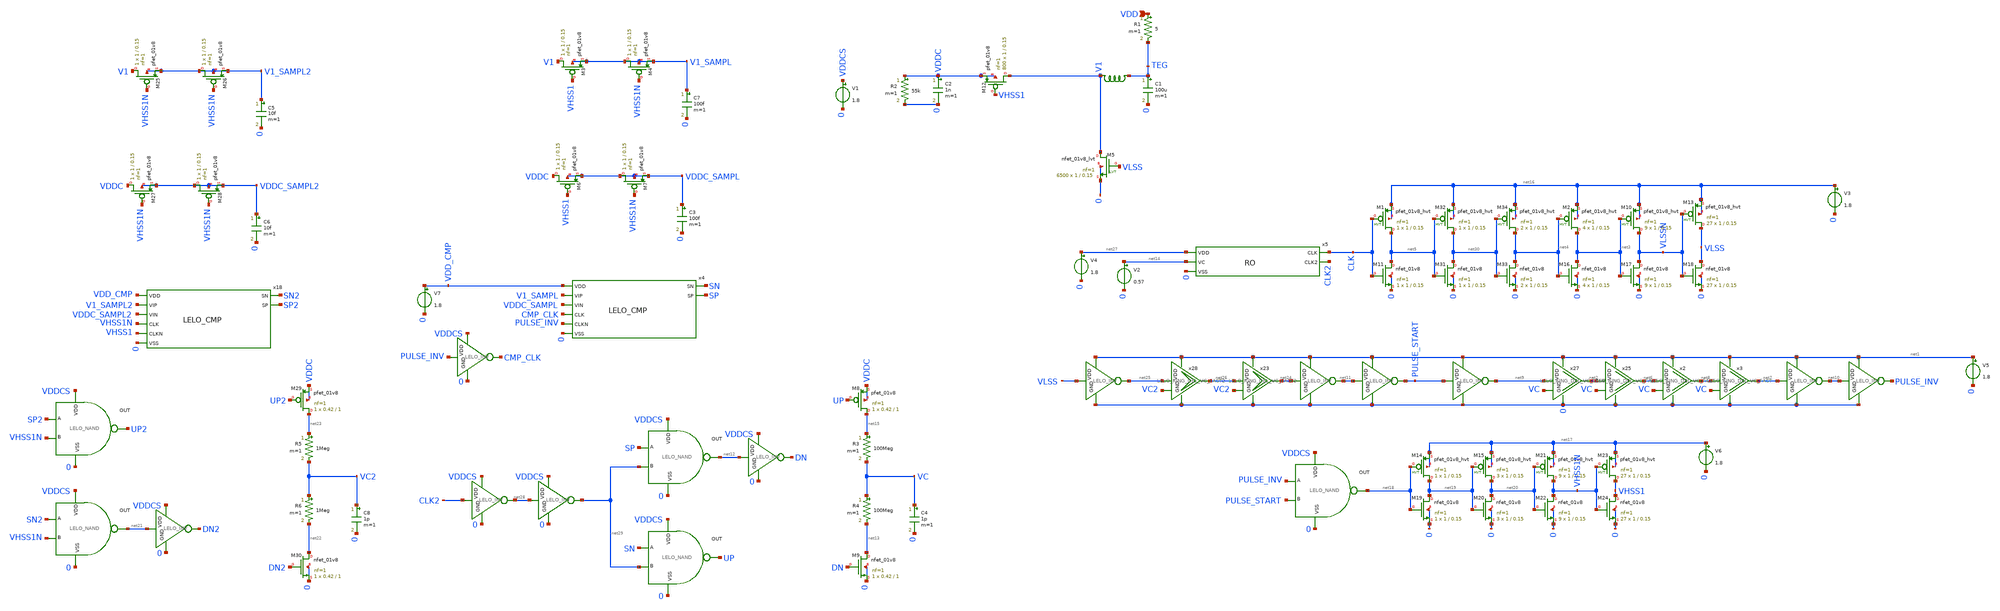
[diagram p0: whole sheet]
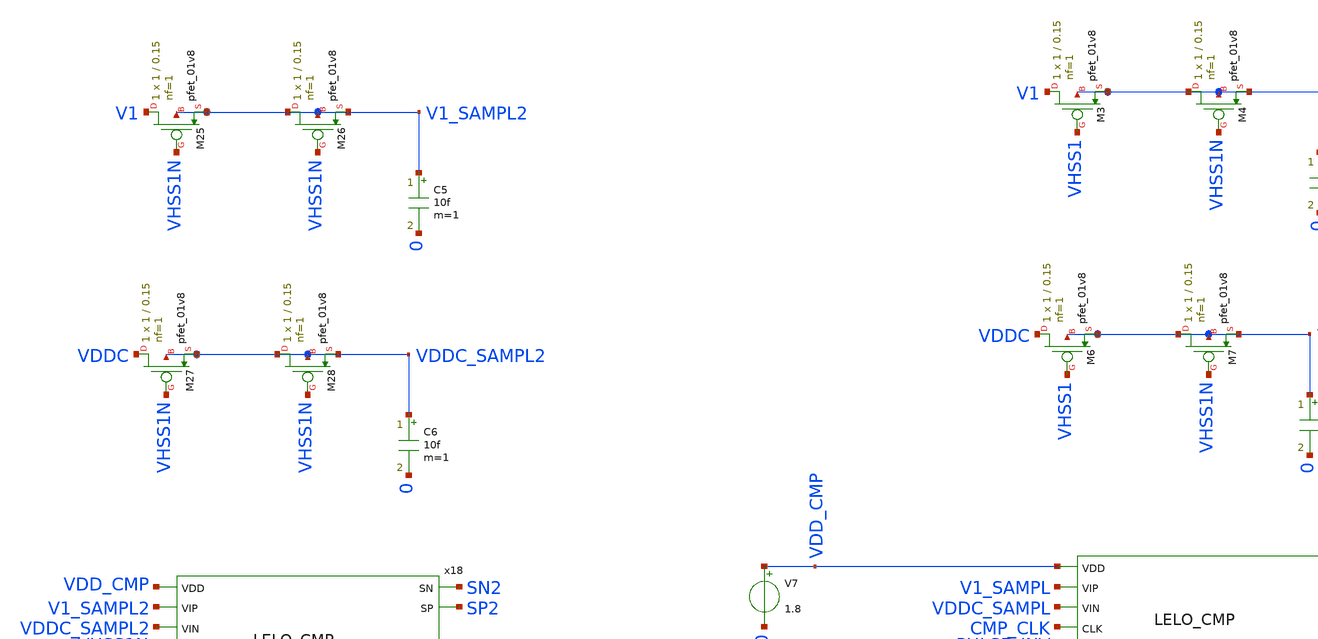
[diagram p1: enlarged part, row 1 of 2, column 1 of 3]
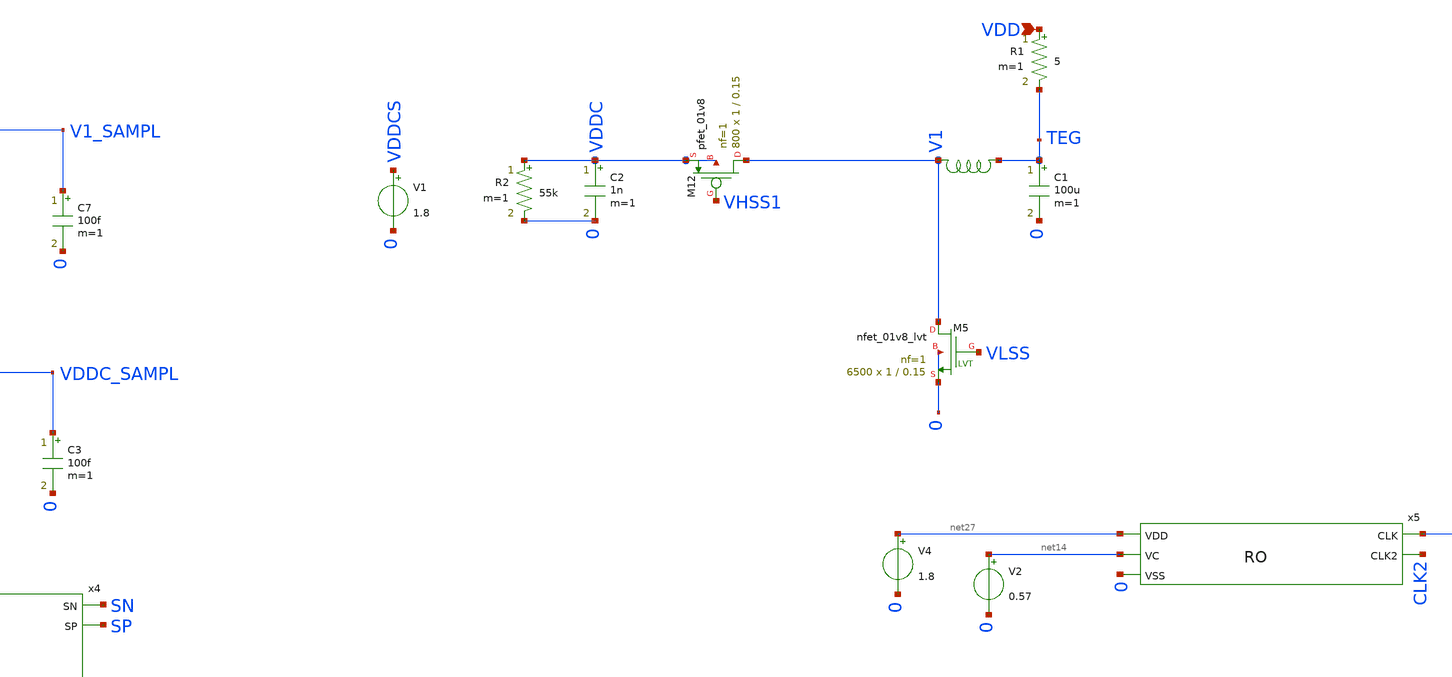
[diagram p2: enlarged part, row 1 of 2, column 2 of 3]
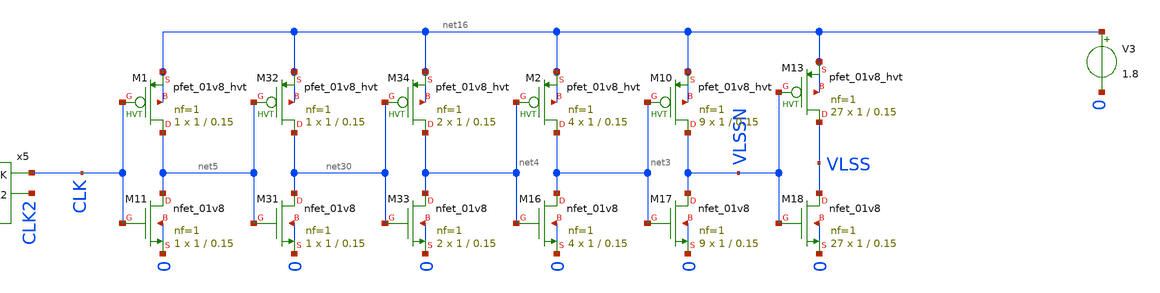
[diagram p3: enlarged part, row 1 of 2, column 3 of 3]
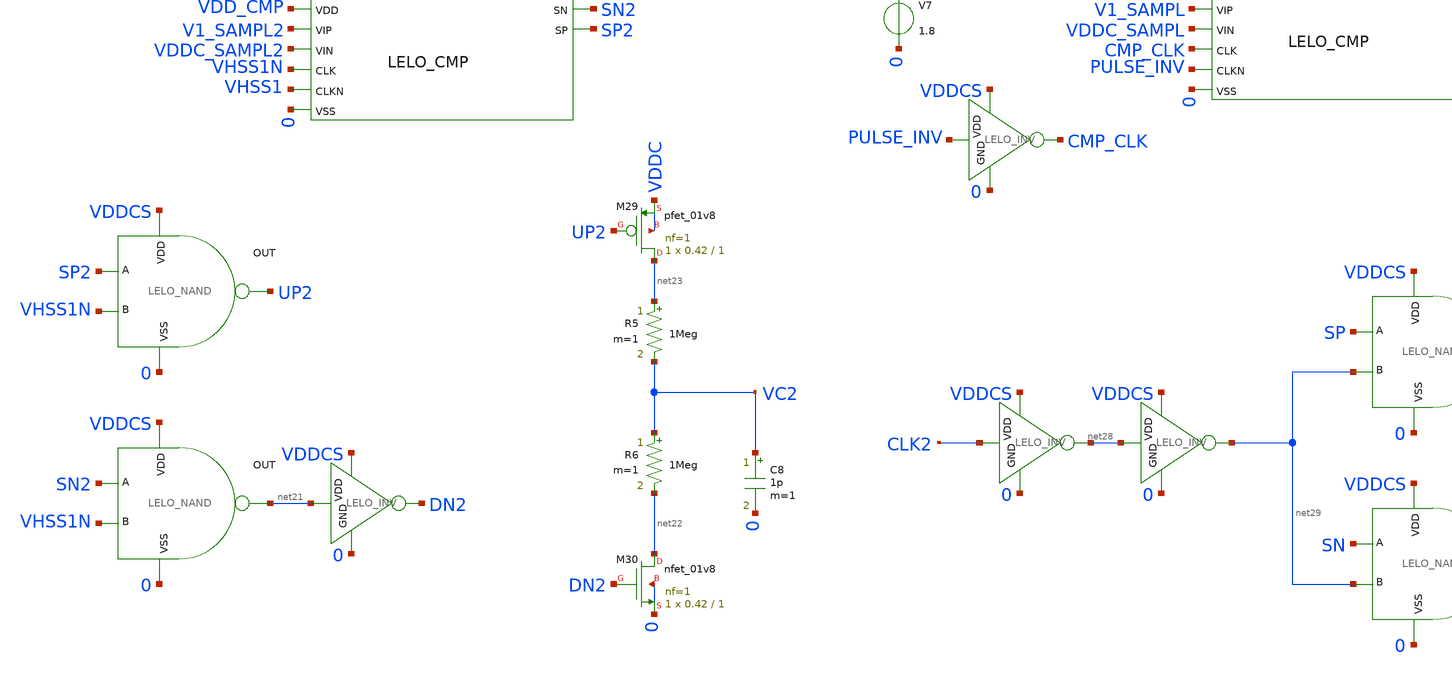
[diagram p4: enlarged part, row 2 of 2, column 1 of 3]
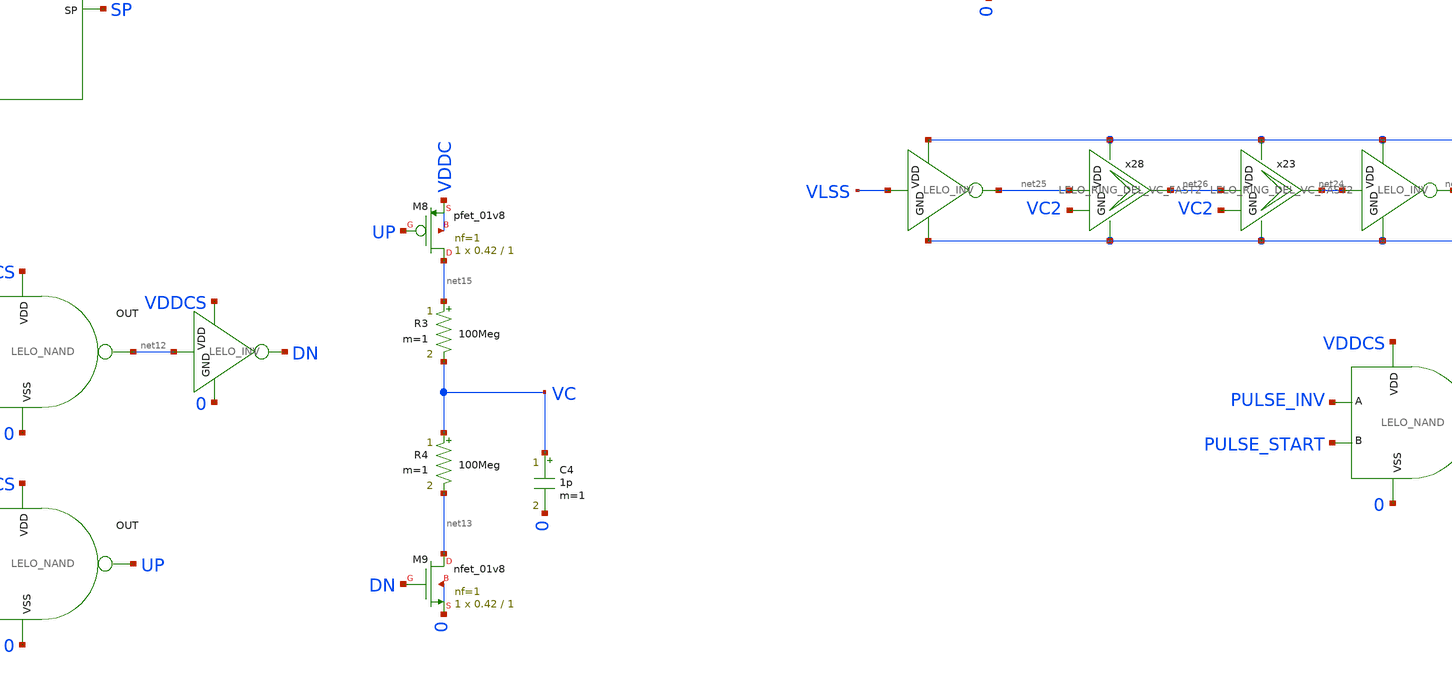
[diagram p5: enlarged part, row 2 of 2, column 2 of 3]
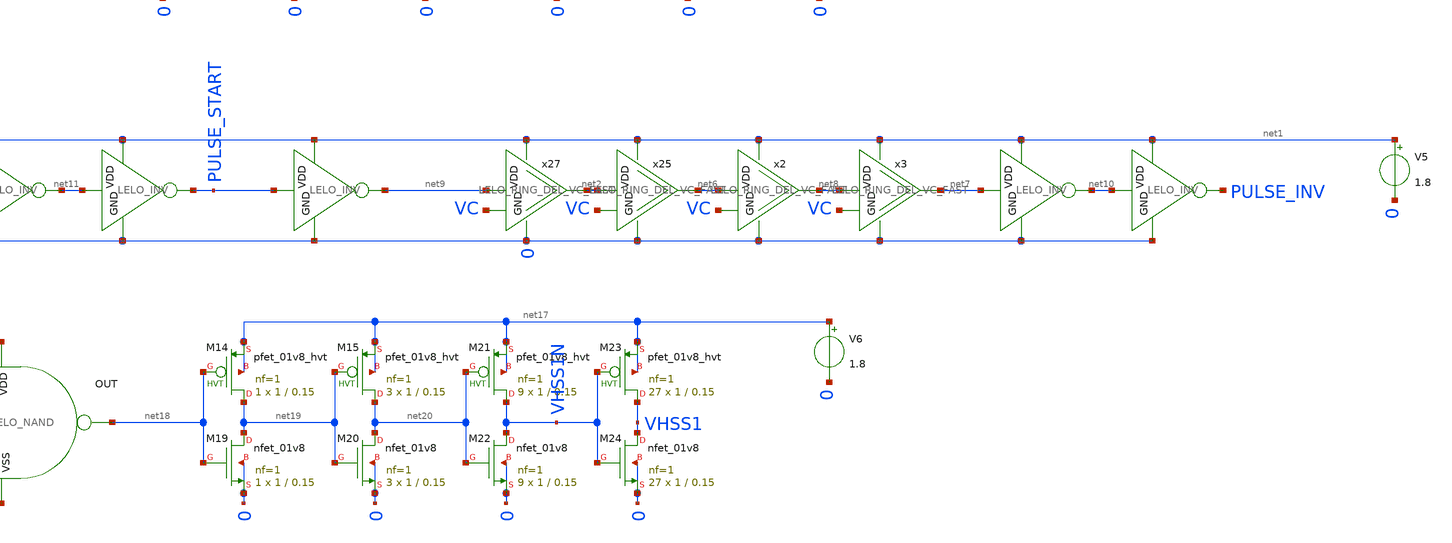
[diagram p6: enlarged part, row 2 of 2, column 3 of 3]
** sch_path: design/LELO_SVOD_SKY130A/LELO_BOOST_STEADY_STATE.sch
**.subckt LELO_BOOST_STEADY_STATE VDD
*.ipin VDD
R1 VDD TEG 5 m=1
C7 V1_SAMPL 0 100f m=1
x8 VDDCS net18 PULSE_INV PULSE_START 0 LELO_NAND
x25 net1 net2 net6 0 VC LELO_RING_DEL_VC_FAST
x6 net1 net7 net10 0 LELO_INV
x27 net1 net9 net2 0 VC LELO_RING_DEL_VC_FAST
x5 CLK CLK2 net27 net14 0 RO
XM12 V1 VHSS1 VDDC VDDC sky130_fd_pr__pfet_01v8 L=0.15 W=1 nf=1 ad='int((1 + 1)/2) * 1 / 1 * 0.29' as='int((1 + 2)/2) * 1 / 1 * 0.29'
+ pd='2*int((1 + 1)/2) * (1 / 1 + 0.29)' ps='2*int((1 + 2)/2) * (1 / 1 + 0.29)' nrd='0.29 / 1 ' nrs='0.29 / 1 '
+ sa=0 sb=0 sd=0 mult=800 m=800
x2 net1 net6 net8 0 VC LELO_RING_DEL_VC_FAST
x3 net1 net8 net7 0 VC LELO_RING_DEL_VC_FAST
x1 net1 net24 net11 0 LELO_INV
x16 net1 net10 PULSE_INV 0 LELO_INV
C1 TEG 0 100u m=1
x9 net1 VLSS net25 0 LELO_INV
XM5 V1 VLSS 0 0 sky130_fd_pr__nfet_01v8_lvt L=0.15 W=1 nf=1 ad='int((1 + 1)/2) * 1 / 1 * 0.29' as='int((1 + 2)/2) * 1 / 1 * 0.29'
+ pd='2*int((1 + 1)/2) * (1 / 1 + 0.29)' ps='2*int((1 + 2)/2) * (1 / 1 + 0.29)' nrd='0.29 / 1 ' nrs='0.29 / 1 '
+ sa=0 sb=0 sd=0 mult=6500 m=6500
C2 VDDC 0 1n m=1
V1 VDDCS 0 1.8
R2 VDDC 0 55k m=1
x4 SN SP VDD_CMP V1_SAMPL VDDC_SAMPL CMP_CLK PULSE_INV 0 LELO_CMP
XM3 V1 VHSS1 V1_SAMPL V1_SAMPL sky130_fd_pr__pfet_01v8 L=0.15 W=1 nf=1 ad='int((1 + 1)/2) * 1 / 1 * 0.29'
+ as='int((1 + 2)/2) * 1 / 1 * 0.29' pd='2*int((1 + 1)/2) * (1 / 1 + 0.29)' ps='2*int((1 + 2)/2) * (1 / 1 + 0.29)'
+ nrd='0.29 / 1 ' nrs='0.29 / 1 ' sa=0 sb=0 sd=0 mult=1 m=1
XM4 V1_SAMPL VHSS1N V1_SAMPL V1_SAMPL sky130_fd_pr__pfet_01v8 L=0.15 W=1 nf=1 ad='int((1 + 1)/2) * 1 / 1 * 0.29'
+ as='int((1 + 2)/2) * 1 / 1 * 0.29' pd='2*int((1 + 1)/2) * (1 / 1 + 0.29)' ps='2*int((1 + 2)/2) * (1 / 1 + 0.29)'
+ nrd='0.29 / 1 ' nrs='0.29 / 1 ' sa=0 sb=0 sd=0 mult=1 m=1
C3 VDDC_SAMPL 0 100f m=1
XM6 VDDC VHSS1 VDDC_SAMPL VDDC_SAMPL sky130_fd_pr__pfet_01v8 L=0.15 W=1 nf=1 ad='int((1 + 1)/2) * 1 / 1 * 0.29'
+ as='int((1 + 2)/2) * 1 / 1 * 0.29' pd='2*int((1 + 1)/2) * (1 / 1 + 0.29)' ps='2*int((1 + 2)/2) * (1 / 1 + 0.29)'
+ nrd='0.29 / 1 ' nrs='0.29 / 1 ' sa=0 sb=0 sd=0 mult=1 m=1
XM7 VDDC_SAMPL VHSS1N VDDC_SAMPL VDDC_SAMPL sky130_fd_pr__pfet_01v8 L=0.15 W=1 nf=1 ad='int((1 + 1)/2) * 1 / 1 * 0.29'
+ as='int((1 + 2)/2) * 1 / 1 * 0.29' pd='2*int((1 + 1)/2) * (1 / 1 + 0.29)' ps='2*int((1 + 2)/2) * (1 / 1 + 0.29)'
+ nrd='0.29 / 1 ' nrs='0.29 / 1 ' sa=0 sb=0 sd=0 mult=1 m=1
C4 VC 0 1p m=1
XM8 net15 UP VDDC VDDC sky130_fd_pr__pfet_01v8 L=1 W=0.42 nf=1 ad='int((1 + 1)/2) * 0.42 / 1 * 0.29'
+ as='int((1 + 2)/2) * 0.42 / 1 * 0.29' pd='2*int((1 + 1)/2) * (0.42 / 1 + 0.29)' ps='2*int((1 + 2)/2) * (0.42 / 1 + 0.29)'
+ nrd='0.29 / 0.42 ' nrs='0.29 / 0.42 ' sa=0 sb=0 sd=0 mult=1 m=1
XM9 net13 DN 0 0 sky130_fd_pr__nfet_01v8 L=1 W=0.42 nf=1 ad='int((1 + 1)/2) * 0.42 / 1 * 0.29' as='int((1 + 2)/2) * 0.42 / 1 * 0.29'
+ pd='2*int((1 + 1)/2) * (0.42 / 1 + 0.29)' ps='2*int((1 + 2)/2) * (0.42 / 1 + 0.29)' nrd='0.29 / 0.42 '
+ nrs='0.29 / 0.42 ' sa=0 sb=0 sd=0 mult=1 m=1
x10 VDDCS net12 SP net29 0 LELO_NAND
x11 VDDCS net12 DN 0 LELO_INV
x12 VDDCS UP SN net29 0 LELO_NAND
V2 net14 0 0.57
x14 VDDCS PULSE_INV CMP_CLK 0 LELO_INV
R3 net15 VC 100Meg m=1
R4 VC net13 100Meg m=1
XM11 net5 CLK 0 0 sky130_fd_pr__nfet_01v8 L=0.15 W=1 nf=1 ad='int((1 + 1)/2) * 1 / 1 * 0.29' as='int((1 + 2)/2) * 1 / 1 * 0.29'
+ pd='2*int((1 + 1)/2) * (1 / 1 + 0.29)' ps='2*int((1 + 2)/2) * (1 / 1 + 0.29)' nrd='0.29 / 1 ' nrs='0.29 / 1 '
+ sa=0 sb=0 sd=0 mult=1 m=1
XM16 net3 net4 0 0 sky130_fd_pr__nfet_01v8 L=0.15 W=1 nf=1 ad='int((1 + 1)/2) * 1 / 1 * 0.29' as='int((1 + 2)/2) * 1 / 1 * 0.29'
+ pd='2*int((1 + 1)/2) * (1 / 1 + 0.29)' ps='2*int((1 + 2)/2) * (1 / 1 + 0.29)' nrd='0.29 / 1 ' nrs='0.29 / 1 '
+ sa=0 sb=0 sd=0 mult=4 m=4
XM17 VLSSN net3 0 0 sky130_fd_pr__nfet_01v8 L=0.15 W=1 nf=1 ad='int((1 + 1)/2) * 1 / 1 * 0.29' as='int((1 + 2)/2) * 1 / 1 * 0.29'
+ pd='2*int((1 + 1)/2) * (1 / 1 + 0.29)' ps='2*int((1 + 2)/2) * (1 / 1 + 0.29)' nrd='0.29 / 1 ' nrs='0.29 / 1 '
+ sa=0 sb=0 sd=0 mult=9 m=9
XM18 VLSS VLSSN 0 0 sky130_fd_pr__nfet_01v8 L=0.15 W=1 nf=1 ad='int((1 + 1)/2) * 1 / 1 * 0.29' as='int((1 + 2)/2) * 1 / 1 * 0.29'
+ pd='2*int((1 + 1)/2) * (1 / 1 + 0.29)' ps='2*int((1 + 2)/2) * (1 / 1 + 0.29)' nrd='0.29 / 1 ' nrs='0.29 / 1 '
+ sa=0 sb=0 sd=0 mult=27 m=27
XM19 net19 net18 0 0 sky130_fd_pr__nfet_01v8 L=0.15 W=1 nf=1 ad='int((1 + 1)/2) * 1 / 1 * 0.29' as='int((1 + 2)/2) * 1 / 1 * 0.29'
+ pd='2*int((1 + 1)/2) * (1 / 1 + 0.29)' ps='2*int((1 + 2)/2) * (1 / 1 + 0.29)' nrd='0.29 / 1 ' nrs='0.29 / 1 '
+ sa=0 sb=0 sd=0 mult=1 m=1
XM20 net20 net19 0 0 sky130_fd_pr__nfet_01v8 L=0.15 W=1 nf=1 ad='int((1 + 1)/2) * 1 / 1 * 0.29' as='int((1 + 2)/2) * 1 / 1 * 0.29'
+ pd='2*int((1 + 1)/2) * (1 / 1 + 0.29)' ps='2*int((1 + 2)/2) * (1 / 1 + 0.29)' nrd='0.29 / 1 ' nrs='0.29 / 1 '
+ sa=0 sb=0 sd=0 mult=3 m=3
XM22 VHSS1N net20 0 0 sky130_fd_pr__nfet_01v8 L=0.15 W=1 nf=1 ad='int((1 + 1)/2) * 1 / 1 * 0.29' as='int((1 + 2)/2) * 1 / 1 * 0.29'
+ pd='2*int((1 + 1)/2) * (1 / 1 + 0.29)' ps='2*int((1 + 2)/2) * (1 / 1 + 0.29)' nrd='0.29 / 1 ' nrs='0.29 / 1 '
+ sa=0 sb=0 sd=0 mult=9 m=9
XM24 VHSS1 VHSS1N 0 0 sky130_fd_pr__nfet_01v8 L=0.15 W=1 nf=1 ad='int((1 + 1)/2) * 1 / 1 * 0.29' as='int((1 + 2)/2) * 1 / 1 * 0.29'
+ pd='2*int((1 + 1)/2) * (1 / 1 + 0.29)' ps='2*int((1 + 2)/2) * (1 / 1 + 0.29)' nrd='0.29 / 1 ' nrs='0.29 / 1 '
+ sa=0 sb=0 sd=0 mult=27 m=27
XM1 net5 CLK net16 net16 sky130_fd_pr__pfet_01v8_hvt L=0.15 W=1 nf=1 ad='int((1 + 1)/2) * 1 / 1 * 0.29'
+ as='int((1 + 2)/2) * 1 / 1 * 0.29' pd='2*int((1 + 1)/2) * (1 / 1 + 0.29)' ps='2*int((1 + 2)/2) * (1 / 1 + 0.29)'
+ nrd='0.29 / 1 ' nrs='0.29 / 1 ' sa=0 sb=0 sd=0 mult=1 m=1
XM2 net3 net4 net16 net16 sky130_fd_pr__pfet_01v8_hvt L=0.15 W=1 nf=1 ad='int((1 + 1)/2) * 1 / 1 * 0.29'
+ as='int((1 + 2)/2) * 1 / 1 * 0.29' pd='2*int((1 + 1)/2) * (1 / 1 + 0.29)' ps='2*int((1 + 2)/2) * (1 / 1 + 0.29)'
+ nrd='0.29 / 1 ' nrs='0.29 / 1 ' sa=0 sb=0 sd=0 mult=4 m=4
XM10 VLSSN net3 net16 net16 sky130_fd_pr__pfet_01v8_hvt L=0.15 W=1 nf=1 ad='int((1 + 1)/2) * 1 / 1 * 0.29'
+ as='int((1 + 2)/2) * 1 / 1 * 0.29' pd='2*int((1 + 1)/2) * (1 / 1 + 0.29)' ps='2*int((1 + 2)/2) * (1 / 1 + 0.29)'
+ nrd='0.29 / 1 ' nrs='0.29 / 1 ' sa=0 sb=0 sd=0 mult=9 m=9
XM13 VLSS VLSSN net16 net16 sky130_fd_pr__pfet_01v8_hvt L=0.15 W=1 nf=1 ad='int((1 + 1)/2) * 1 / 1 * 0.29'
+ as='int((1 + 2)/2) * 1 / 1 * 0.29' pd='2*int((1 + 1)/2) * (1 / 1 + 0.29)' ps='2*int((1 + 2)/2) * (1 / 1 + 0.29)'
+ nrd='0.29 / 1 ' nrs='0.29 / 1 ' sa=0 sb=0 sd=0 mult=27 m=27
XM14 net19 net18 net17 net17 sky130_fd_pr__pfet_01v8_hvt L=0.15 W=1 nf=1 ad='int((1 + 1)/2) * 1 / 1 * 0.29'
+ as='int((1 + 2)/2) * 1 / 1 * 0.29' pd='2*int((1 + 1)/2) * (1 / 1 + 0.29)' ps='2*int((1 + 2)/2) * (1 / 1 + 0.29)'
+ nrd='0.29 / 1 ' nrs='0.29 / 1 ' sa=0 sb=0 sd=0 mult=1 m=1
XM15 net20 net19 net17 net17 sky130_fd_pr__pfet_01v8_hvt L=0.15 W=1 nf=1 ad='int((1 + 1)/2) * 1 / 1 * 0.29'
+ as='int((1 + 2)/2) * 1 / 1 * 0.29' pd='2*int((1 + 1)/2) * (1 / 1 + 0.29)' ps='2*int((1 + 2)/2) * (1 / 1 + 0.29)'
+ nrd='0.29 / 1 ' nrs='0.29 / 1 ' sa=0 sb=0 sd=0 mult=3 m=3
XM21 VHSS1N net20 net17 net17 sky130_fd_pr__pfet_01v8_hvt L=0.15 W=1 nf=1 ad='int((1 + 1)/2) * 1 / 1 * 0.29'
+ as='int((1 + 2)/2) * 1 / 1 * 0.29' pd='2*int((1 + 1)/2) * (1 / 1 + 0.29)' ps='2*int((1 + 2)/2) * (1 / 1 + 0.29)'
+ nrd='0.29 / 1 ' nrs='0.29 / 1 ' sa=0 sb=0 sd=0 mult=9 m=9
XM23 VHSS1 VHSS1N net17 net17 sky130_fd_pr__pfet_01v8_hvt L=0.15 W=1 nf=1 ad='int((1 + 1)/2) * 1 / 1 * 0.29'
+ as='int((1 + 2)/2) * 1 / 1 * 0.29' pd='2*int((1 + 1)/2) * (1 / 1 + 0.29)' ps='2*int((1 + 2)/2) * (1 / 1 + 0.29)'
+ nrd='0.29 / 1 ' nrs='0.29 / 1 ' sa=0 sb=0 sd=0 mult=27 m=27
C5 V1_SAMPL2 0 10f m=1
x18 SN2 SP2 VDD_CMP V1_SAMPL2 VDDC_SAMPL2 VHSS1N VHSS1 0 LELO_CMP
XM25 V1 VHSS1N V1_SAMPL2 V1_SAMPL2 sky130_fd_pr__pfet_01v8 L=0.15 W=1 nf=1 ad='int((1 + 1)/2) * 1 / 1 * 0.29'
+ as='int((1 + 2)/2) * 1 / 1 * 0.29' pd='2*int((1 + 1)/2) * (1 / 1 + 0.29)' ps='2*int((1 + 2)/2) * (1 / 1 + 0.29)'
+ nrd='0.29 / 1 ' nrs='0.29 / 1 ' sa=0 sb=0 sd=0 mult=1 m=1
XM26 V1_SAMPL2 VHSS1N V1_SAMPL2 V1_SAMPL2 sky130_fd_pr__pfet_01v8 L=0.15 W=1 nf=1 ad='int((1 + 1)/2) * 1 / 1 * 0.29'
+ as='int((1 + 2)/2) * 1 / 1 * 0.29' pd='2*int((1 + 1)/2) * (1 / 1 + 0.29)' ps='2*int((1 + 2)/2) * (1 / 1 + 0.29)'
+ nrd='0.29 / 1 ' nrs='0.29 / 1 ' sa=0 sb=0 sd=0 mult=1 m=1
C6 VDDC_SAMPL2 0 10f m=1
XM27 VDDC VHSS1N VDDC_SAMPL2 VDDC_SAMPL2 sky130_fd_pr__pfet_01v8 L=0.15 W=1 nf=1 ad='int((1 + 1)/2) * 1 / 1 * 0.29'
+ as='int((1 + 2)/2) * 1 / 1 * 0.29' pd='2*int((1 + 1)/2) * (1 / 1 + 0.29)' ps='2*int((1 + 2)/2) * (1 / 1 + 0.29)'
+ nrd='0.29 / 1 ' nrs='0.29 / 1 ' sa=0 sb=0 sd=0 mult=1 m=1
XM28 VDDC_SAMPL2 VHSS1N VDDC_SAMPL2 VDDC_SAMPL2 sky130_fd_pr__pfet_01v8 L=0.15 W=1 nf=1 ad='int((1 + 1)/2) * 1 / 1 * 0.29'
+ as='int((1 + 2)/2) * 1 / 1 * 0.29' pd='2*int((1 + 1)/2) * (1 / 1 + 0.29)' ps='2*int((1 + 2)/2) * (1 / 1 + 0.29)'
+ nrd='0.29 / 1 ' nrs='0.29 / 1 ' sa=0 sb=0 sd=0 mult=1 m=1
x19 VDDCS UP2 SP2 VHSS1N 0 LELO_NAND
x20 VDDCS net21 DN2 0 LELO_INV
x21 VDDCS net21 SN2 VHSS1N 0 LELO_NAND
C8 VC2 0 1p m=1
XM29 net23 UP2 VDDC VDDC sky130_fd_pr__pfet_01v8 L=1 W=0.42 nf=1 ad='int((1 + 1)/2) * 0.42 / 1 * 0.29'
+ as='int((1 + 2)/2) * 0.42 / 1 * 0.29' pd='2*int((1 + 1)/2) * (0.42 / 1 + 0.29)' ps='2*int((1 + 2)/2) * (0.42 / 1 + 0.29)'
+ nrd='0.29 / 0.42 ' nrs='0.29 / 0.42 ' sa=0 sb=0 sd=0 mult=1 m=1
XM30 net22 DN2 0 0 sky130_fd_pr__nfet_01v8 L=1 W=0.42 nf=1 ad='int((1 + 1)/2) * 0.42 / 1 * 0.29' as='int((1 + 2)/2) * 0.42 / 1 * 0.29'
+ pd='2*int((1 + 1)/2) * (0.42 / 1 + 0.29)' ps='2*int((1 + 2)/2) * (0.42 / 1 + 0.29)' nrd='0.29 / 0.42 '
+ nrs='0.29 / 0.42 ' sa=0 sb=0 sd=0 mult=1 m=1
R5 net23 VC2 1Meg m=1
R6 VC2 net22 1Meg m=1
x23 net1 net26 net24 0 VC2 LELO_RING_DEL_VC_FAST2
x28 net1 net25 net26 0 VC2 LELO_RING_DEL_VC_FAST2
V4 net27 0 1.8
V3 net16 0 1.8
V5 net1 0 1.8
V6 net17 0 1.8
V7 VDD_CMP 0 1.8
x13 VDDCS net28 net29 0 LELO_INV
x15 VDDCS CLK2 net28 0 LELO_INV
x17 net1 net11 PULSE_START 0 LELO_INV
x22 net1 PULSE_START net9 0 LELO_INV
XM31 net30 net5 0 0 sky130_fd_pr__nfet_01v8 L=0.15 W=1 nf=1 ad='int((1 + 1)/2) * 1 / 1 * 0.29' as='int((1 + 2)/2) * 1 / 1 * 0.29'
+ pd='2*int((1 + 1)/2) * (1 / 1 + 0.29)' ps='2*int((1 + 2)/2) * (1 / 1 + 0.29)' nrd='0.29 / 1 ' nrs='0.29 / 1 '
+ sa=0 sb=0 sd=0 mult=1 m=1
XM32 net30 net5 net16 net16 sky130_fd_pr__pfet_01v8_hvt L=0.15 W=1 nf=1 ad='int((1 + 1)/2) * 1 / 1 * 0.29'
+ as='int((1 + 2)/2) * 1 / 1 * 0.29' pd='2*int((1 + 1)/2) * (1 / 1 + 0.29)' ps='2*int((1 + 2)/2) * (1 / 1 + 0.29)'
+ nrd='0.29 / 1 ' nrs='0.29 / 1 ' sa=0 sb=0 sd=0 mult=1 m=1
XM33 net4 net30 0 0 sky130_fd_pr__nfet_01v8 L=0.15 W=1 nf=1 ad='int((1 + 1)/2) * 1 / 1 * 0.29' as='int((1 + 2)/2) * 1 / 1 * 0.29'
+ pd='2*int((1 + 1)/2) * (1 / 1 + 0.29)' ps='2*int((1 + 2)/2) * (1 / 1 + 0.29)' nrd='0.29 / 1 ' nrs='0.29 / 1 '
+ sa=0 sb=0 sd=0 mult=2 m=2
XM34 net4 net30 net16 net16 sky130_fd_pr__pfet_01v8_hvt L=0.15 W=1 nf=1 ad='int((1 + 1)/2) * 1 / 1 * 0.29'
+ as='int((1 + 2)/2) * 1 / 1 * 0.29' pd='2*int((1 + 1)/2) * (1 / 1 + 0.29)' ps='2*int((1 + 2)/2) * (1 / 1 + 0.29)'
+ nrd='0.29 / 1 ' nrs='0.29 / 1 ' sa=0 sb=0 sd=0 mult=2 m=2
x7 TEG V1 XGL6030-822_sat
**.ends

* expanding   symbol:  LELO_SVOD_SKY130A/LELO_NAND.sym # of pins=5
** sym_path: design/LELO_SVOD_SKY130A/LELO_NAND.sym
** sch_path: design/LELO_SVOD_SKY130A/LELO_NAND.sch
.subckt LELO_NAND VDD OUT A B VSS
*.ipin VDD
*.ipin VSS
*.opin OUT
*.ipin A
*.ipin B
XM1 net1 A VSS VSS sky130_fd_pr__nfet_01v8_lvt L=0.15 W=1 nf=1 ad='int((1 + 1)/2) * 1 / 1 * 0.29' as='int((1 + 2)/2) * 1 / 1 * 0.29'
+ pd='2*int((1 + 1)/2) * (1 / 1 + 0.29)' ps='2*int((1 + 2)/2) * (1 / 1 + 0.29)' nrd='0.29 / 1 ' nrs='0.29 / 1 '
+ sa=0 sb=0 sd=0 mult=1 m=1
XM2 OUT B net1 net1 sky130_fd_pr__nfet_01v8_lvt L=0.15 W=1 nf=1 ad='int((1 + 1)/2) * 1 / 1 * 0.29' as='int((1 + 2)/2) * 1 / 1 * 0.29'
+ pd='2*int((1 + 1)/2) * (1 / 1 + 0.29)' ps='2*int((1 + 2)/2) * (1 / 1 + 0.29)' nrd='0.29 / 1 ' nrs='0.29 / 1 '
+ sa=0 sb=0 sd=0 mult=1 m=1
XM3 OUT A VDD VDD sky130_fd_pr__pfet_01v8_lvt L=0.35 W=1 nf=1 ad='int((1 + 1)/2) * 1 / 1 * 0.29' as='int((1 + 2)/2) * 1 / 1 * 0.29'
+ pd='2*int((1 + 1)/2) * (1 / 1 + 0.29)' ps='2*int((1 + 2)/2) * (1 / 1 + 0.29)' nrd='0.29 / 1 ' nrs='0.29 / 1 '
+ sa=0 sb=0 sd=0 mult=1 m=1
XM4 OUT B VDD VDD sky130_fd_pr__pfet_01v8_lvt L=0.35 W=1 nf=1 ad='int((1 + 1)/2) * 1 / 1 * 0.29' as='int((1 + 2)/2) * 1 / 1 * 0.29'
+ pd='2*int((1 + 1)/2) * (1 / 1 + 0.29)' ps='2*int((1 + 2)/2) * (1 / 1 + 0.29)' nrd='0.29 / 1 ' nrs='0.29 / 1 '
+ sa=0 sb=0 sd=0 mult=1 m=1
.ends


* expanding   symbol:  LELO_SVOD_SKY130A/LELO_RING_DEL_VC_FAST.sym # of pins=5
** sym_path: design/LELO_SVOD_SKY130A/LELO_RING_DEL_VC_FAST.sym
** sch_path: design/LELO_SVOD_SKY130A/LELO_RING_DEL_VC_FAST.sch
.subckt LELO_RING_DEL_VC_FAST VDD VIN VOUT GND VC
*.ipin VIN
*.ipin VDD
*.opin VOUT
*.ipin VC
*.ipin GND
XM4 net1 VC GND GND sky130_fd_pr__nfet_01v8 L=0.15 W=6 nf=1 ad='int((1 + 1)/2) * 6 / 1 * 0.29' as='int((1 + 2)/2) * 6 / 1 * 0.29'
+ pd='2*int((1 + 1)/2) * (6 / 1 + 0.29)' ps='2*int((1 + 2)/2) * (6 / 1 + 0.29)' nrd='0.29 / 6 ' nrs='0.29 / 6 '
+ sa=0 sb=0 sd=0 mult=1 m=1
XM3 net1 VIN GND GND sky130_fd_pr__nfet_01v8 L=8 W=0.42 nf=1 ad='int((1 + 1)/2) * 0.42 / 1 * 0.29' as='int((1 + 2)/2) * 0.42 / 1 * 0.29'
+ pd='2*int((1 + 1)/2) * (0.42 / 1 + 0.29)' ps='2*int((1 + 2)/2) * (0.42 / 1 + 0.29)' nrd='0.29 / 0.42 '
+ nrs='0.29 / 0.42 ' sa=0 sb=0 sd=0 mult=1 m=1
XM1 VOUT VIN net1 GND sky130_fd_pr__nfet_01v8 L=1 W=3 nf=1 ad='int((1 + 1)/2) * 3 / 1 * 0.29' as='int((1 + 2)/2) * 3 / 1 * 0.29'
+ pd='2*int((1 + 1)/2) * (3 / 1 + 0.29)' ps='2*int((1 + 2)/2) * (3 / 1 + 0.29)' nrd='0.29 / 3 ' nrs='0.29 / 3 '
+ sa=0 sb=0 sd=0 mult=1 m=1
XM2 VOUT VIN VDD VDD sky130_fd_pr__pfet_01v8 L=2 W=0.42 nf=1 ad='int((1 + 1)/2) * 0.42 / 1 * 0.29' as='int((1 + 2)/2) * 0.42 / 1 * 0.29'
+ pd='2*int((1 + 1)/2) * (0.42 / 1 + 0.29)' ps='2*int((1 + 2)/2) * (0.42 / 1 + 0.29)' nrd='0.29 / 0.42 '
+ nrs='0.29 / 0.42 ' sa=0 sb=0 sd=0 mult=1 m=1
.ends


* expanding   symbol:  LELO_SVOD_SKY130A/LELO_INV.sym # of pins=4
** sym_path: design/LELO_SVOD_SKY130A/LELO_INV.sym
** sch_path: design/LELO_SVOD_SKY130A/LELO_INV.sch
.subckt LELO_INV VDD VIN VOUT GND
*.ipin VIN
*.ipin VDD
*.ipin GND
*.opin VOUT
XM1 VOUT VIN VDD VDD sky130_fd_pr__pfet_01v8_hvt L=0.15 W=0.42 nf=1 ad='int((1 + 1)/2) * 0.42 / 1 * 0.29'
+ as='int((1 + 2)/2) * 0.42 / 1 * 0.29' pd='2*int((1 + 1)/2) * (0.42 / 1 + 0.29)' ps='2*int((1 + 2)/2) * (0.42 / 1 + 0.29)'
+ nrd='0.29 / 0.42 ' nrs='0.29 / 0.42 ' sa=0 sb=0 sd=0 mult=1 m=1
XM2 VOUT VIN GND GND sky130_fd_pr__nfet_01v8 L=0.15 W=0.42 nf=1 ad='int((1 + 1)/2) * 0.42 / 1 * 0.29'
+ as='int((1 + 2)/2) * 0.42 / 1 * 0.29' pd='2*int((1 + 1)/2) * (0.42 / 1 + 0.29)' ps='2*int((1 + 2)/2) * (0.42 / 1 + 0.29)'
+ nrd='0.29 / 0.42 ' nrs='0.29 / 0.42 ' sa=0 sb=0 sd=0 mult=1 m=1
.ends


* expanding   symbol:  LELO_SVOD_SKY130A/RO.sym # of pins=5
** sym_path: design/LELO_SVOD_SKY130A/RO.sym
** sch_path: design/LELO_SVOD_SKY130A/RO.sch
.subckt RO CLK CLK2 VDD VC VSS
*.opin CLK
*.ipin VSS
*.opin CLK2
*.ipin VDD
*.ipin VC
x1 VDD VC2 CLK net1 VC VSS LELO_RING_DEL_VC
x2 VDD VC2 net1 CLK2 VC VSS LELO_RING_DEL_VC
x3 VDD VC2 CLK2 net2 VC VSS LELO_RING_DEL_VC
x4 VDD VC2 net2 net3 VC VSS LELO_RING_DEL_VC
x5 VDD VC2 net3 net4 VC VSS LELO_RING_DEL_VC
x6 VDD VC2 net4 net5 VC VSS LELO_RING_DEL_VC
x7 VDD VC2 net5 CLK VC VSS LELO_RING_DEL_VC
XM1 VC2 VC VSS VSS sky130_fd_pr__nfet_01v8 L=5 W=0.42 nf=1 ad='int((1 + 1)/2) * 0.42 / 1 * 0.29' as='int((1 + 2)/2) * 0.42 / 1 * 0.29'
+ pd='2*int((1 + 1)/2) * (0.42 / 1 + 0.29)' ps='2*int((1 + 2)/2) * (0.42 / 1 + 0.29)' nrd='0.29 / 0.42 '
+ nrs='0.29 / 0.42 ' sa=0 sb=0 sd=0 mult=1 m=1
XM2 VC2 VC2 VDD VDD sky130_fd_pr__pfet_01v8 L=5 W=0.42 nf=1 ad='int((1 + 1)/2) * 0.42 / 1 * 0.29' as='int((1 + 2)/2) * 0.42 / 1 * 0.29'
+ pd='2*int((1 + 1)/2) * (0.42 / 1 + 0.29)' ps='2*int((1 + 2)/2) * (0.42 / 1 + 0.29)' nrd='0.29 / 0.42 '
+ nrs='0.29 / 0.42 ' sa=0 sb=0 sd=0 mult=1 m=1
.ends


* expanding   symbol:  LELO_SVOD_SKY130A/LELO_CMP.sym # of pins=8
** sym_path: design/LELO_SVOD_SKY130A/LELO_CMP.sym
** sch_path: design/LELO_SVOD_SKY130A/LELO_CMP.sch
.subckt LELO_CMP SN SP VDD VIP VIN CLK CLKN VSS
*.ipin VIP
*.ipin VIN
*.ipin CLK
*.ipin CLKN
*.ipin VDD
*.ipin VSS
*.opin SN
*.opin SP
XM2 SN net3 net5 VDD sky130_fd_pr__pfet_01v8_lvt L=0.44 W=1.92 nf=2 ad='int((2 + 1)/2) * 1.92 / 2 * 0.29'
+ as='int((2 + 2)/2) * 1.92 / 2 * 0.29' pd='2*int((2 + 1)/2) * (1.92 / 2 + 0.29)' ps='2*int((2 + 2)/2) * (1.92 / 2 + 0.29)'
+ nrd='0.29 / 1.92 ' nrs='0.29 / 1.92 ' sa=0 sb=0 sd=0 mult=3 m=3
XM1 SP net2 net6 VDD sky130_fd_pr__pfet_01v8_lvt L=0.44 W=1.92 nf=2 ad='int((2 + 1)/2) * 1.92 / 2 * 0.29'
+ as='int((2 + 2)/2) * 1.92 / 2 * 0.29' pd='2*int((2 + 1)/2) * (1.92 / 2 + 0.29)' ps='2*int((2 + 2)/2) * (1.92 / 2 + 0.29)'
+ nrd='0.29 / 1.92 ' nrs='0.29 / 1.92 ' sa=0 sb=0 sd=0 mult=3 m=3
XM3 net2 VIP net1 VSS sky130_fd_pr__nfet_01v8_lvt L=0.44 W=6.4 nf=1 ad='int((1 + 1)/2) * 6.4 / 1 * 0.29'
+ as='int((1 + 2)/2) * 6.4 / 1 * 0.29' pd='2*int((1 + 1)/2) * (6.4 / 1 + 0.29)' ps='2*int((1 + 2)/2) * (6.4 / 1 + 0.29)'
+ nrd='0.29 / 6.4 ' nrs='0.29 / 6.4 ' sa=0 sb=0 sd=0 mult=1 m=1
XM4 net3 VIN net1 VSS sky130_fd_pr__nfet_01v8_lvt L=0.44 W=6.4 nf=1 ad='int((1 + 1)/2) * 6.4 / 1 * 0.29'
+ as='int((1 + 2)/2) * 6.4 / 1 * 0.29' pd='2*int((1 + 1)/2) * (6.4 / 1 + 0.29)' ps='2*int((1 + 2)/2) * (6.4 / 1 + 0.29)'
+ nrd='0.29 / 6.4 ' nrs='0.29 / 6.4 ' sa=0 sb=0 sd=0 mult=1 m=1
XM5 net3 CLK VDD VDD sky130_fd_pr__pfet_01v8_lvt L=0.94 W=1.92 nf=2 ad='int((2 + 1)/2) * 1.92 / 2 * 0.29'
+ as='int((2 + 2)/2) * 1.92 / 2 * 0.29' pd='2*int((2 + 1)/2) * (1.92 / 2 + 0.29)' ps='2*int((2 + 2)/2) * (1.92 / 2 + 0.29)'
+ nrd='0.29 / 1.92 ' nrs='0.29 / 1.92 ' sa=0 sb=0 sd=0 mult=1 m=1
XM6 net6 SN VDD VDD sky130_fd_pr__pfet_01v8_lvt L=0.94 W=1.92 nf=2 ad='int((2 + 1)/2) * 1.92 / 2 * 0.29'
+ as='int((2 + 2)/2) * 1.92 / 2 * 0.29' pd='2*int((2 + 1)/2) * (1.92 / 2 + 0.29)' ps='2*int((2 + 2)/2) * (1.92 / 2 + 0.29)'
+ nrd='0.29 / 1.92 ' nrs='0.29 / 1.92 ' sa=0 sb=0 sd=0 mult=1 m=1
XM7 net5 SP VDD VDD sky130_fd_pr__pfet_01v8_lvt L=0.94 W=1.92 nf=2 ad='int((2 + 1)/2) * 1.92 / 2 * 0.29'
+ as='int((2 + 2)/2) * 1.92 / 2 * 0.29' pd='2*int((2 + 1)/2) * (1.92 / 2 + 0.29)' ps='2*int((2 + 2)/2) * (1.92 / 2 + 0.29)'
+ nrd='0.29 / 1.92 ' nrs='0.29 / 1.92 ' sa=0 sb=0 sd=0 mult=1 m=1
XM8 net2 CLK VDD VDD sky130_fd_pr__pfet_01v8_lvt L=0.94 W=1.92 nf=2 ad='int((2 + 1)/2) * 1.92 / 2 * 0.29'
+ as='int((2 + 2)/2) * 1.92 / 2 * 0.29' pd='2*int((2 + 1)/2) * (1.92 / 2 + 0.29)' ps='2*int((2 + 2)/2) * (1.92 / 2 + 0.29)'
+ nrd='0.29 / 1.92 ' nrs='0.29 / 1.92 ' sa=0 sb=0 sd=0 mult=1 m=1
XM9 net1 CLK net4 VSS sky130_fd_pr__nfet_01v8 L=0.94 W=1.92 nf=2 ad='int((2 + 1)/2) * 1.92 / 2 * 0.29'
+ as='int((2 + 2)/2) * 1.92 / 2 * 0.29' pd='2*int((2 + 1)/2) * (1.92 / 2 + 0.29)' ps='2*int((2 + 2)/2) * (1.92 / 2 + 0.29)'
+ nrd='0.29 / 1.92 ' nrs='0.29 / 1.92 ' sa=0 sb=0 sd=0 mult=1 m=1
XM10 net4 CLK VSS VSS sky130_fd_pr__nfet_01v8 L=0.94 W=1.92 nf=2 ad='int((2 + 1)/2) * 1.92 / 2 * 0.29'
+ as='int((2 + 2)/2) * 1.92 / 2 * 0.29' pd='2*int((2 + 1)/2) * (1.92 / 2 + 0.29)' ps='2*int((2 + 2)/2) * (1.92 / 2 + 0.29)'
+ nrd='0.29 / 1.92 ' nrs='0.29 / 1.92 ' sa=0 sb=0 sd=0 mult=1 m=1
XM11 SN CLKN VSS VSS sky130_fd_pr__nfet_01v8 L=0.94 W=1.92 nf=2 ad='int((2 + 1)/2) * 1.92 / 2 * 0.29'
+ as='int((2 + 2)/2) * 1.92 / 2 * 0.29' pd='2*int((2 + 1)/2) * (1.92 / 2 + 0.29)' ps='2*int((2 + 2)/2) * (1.92 / 2 + 0.29)'
+ nrd='0.29 / 1.92 ' nrs='0.29 / 1.92 ' sa=0 sb=0 sd=0 mult=1 m=1
XM12 SP SN VSS VSS sky130_fd_pr__nfet_01v8 L=0.94 W=1.92 nf=2 ad='int((2 + 1)/2) * 1.92 / 2 * 0.29' as='int((2 + 2)/2) * 1.92 / 2 * 0.29'
+ pd='2*int((2 + 1)/2) * (1.92 / 2 + 0.29)' ps='2*int((2 + 2)/2) * (1.92 / 2 + 0.29)' nrd='0.29 / 1.92 '
+ nrs='0.29 / 1.92 ' sa=0 sb=0 sd=0 mult=1 m=1
XM13 SN SP VSS VSS sky130_fd_pr__nfet_01v8 L=0.94 W=1.92 nf=2 ad='int((2 + 1)/2) * 1.92 / 2 * 0.29' as='int((2 + 2)/2) * 1.92 / 2 * 0.29'
+ pd='2*int((2 + 1)/2) * (1.92 / 2 + 0.29)' ps='2*int((2 + 2)/2) * (1.92 / 2 + 0.29)' nrd='0.29 / 1.92 '
+ nrs='0.29 / 1.92 ' sa=0 sb=0 sd=0 mult=1 m=1
XM14 SP CLKN VSS VSS sky130_fd_pr__nfet_01v8 L=0.94 W=1.92 nf=2 ad='int((2 + 1)/2) * 1.92 / 2 * 0.29'
+ as='int((2 + 2)/2) * 1.92 / 2 * 0.29' pd='2*int((2 + 1)/2) * (1.92 / 2 + 0.29)' ps='2*int((2 + 2)/2) * (1.92 / 2 + 0.29)'
+ nrd='0.29 / 1.92 ' nrs='0.29 / 1.92 ' sa=0 sb=0 sd=0 mult=1 m=1
.ends


* expanding   symbol:  LELO_SVOD_SKY130A/LELO_RING_DEL_VC_FAST2.sym # of pins=5
** sym_path: design/LELO_SVOD_SKY130A/LELO_RING_DEL_VC_FAST2.sym
** sch_path: design/LELO_SVOD_SKY130A/LELO_RING_DEL_VC_FAST2.sch
.subckt LELO_RING_DEL_VC_FAST2 VDD VIN VOUT GND VC
*.ipin VIN
*.ipin VDD
*.opin VOUT
*.ipin VC
*.ipin GND
XM4 net1 VC GND GND sky130_fd_pr__nfet_01v8 L=0.15 W=6 nf=1 ad='int((1 + 1)/2) * 6 / 1 * 0.29' as='int((1 + 2)/2) * 6 / 1 * 0.29'
+ pd='2*int((1 + 1)/2) * (6 / 1 + 0.29)' ps='2*int((1 + 2)/2) * (6 / 1 + 0.29)' nrd='0.29 / 6 ' nrs='0.29 / 6 '
+ sa=0 sb=0 sd=0 mult=1 m=1
XM3 net1 VIN GND GND sky130_fd_pr__nfet_01v8 L=2 W=0.42 nf=1 ad='int((1 + 1)/2) * 0.42 / 1 * 0.29' as='int((1 + 2)/2) * 0.42 / 1 * 0.29'
+ pd='2*int((1 + 1)/2) * (0.42 / 1 + 0.29)' ps='2*int((1 + 2)/2) * (0.42 / 1 + 0.29)' nrd='0.29 / 0.42 '
+ nrs='0.29 / 0.42 ' sa=0 sb=0 sd=0 mult=1 m=1
XM1 VOUT VIN net1 GND sky130_fd_pr__nfet_01v8 L=1 W=3 nf=1 ad='int((1 + 1)/2) * 3 / 1 * 0.29' as='int((1 + 2)/2) * 3 / 1 * 0.29'
+ pd='2*int((1 + 1)/2) * (3 / 1 + 0.29)' ps='2*int((1 + 2)/2) * (3 / 1 + 0.29)' nrd='0.29 / 3 ' nrs='0.29 / 3 '
+ sa=0 sb=0 sd=0 mult=1 m=1
XM2 VOUT VIN VDD VDD sky130_fd_pr__pfet_01v8 L=0.15 W=0.42 nf=1 ad='int((1 + 1)/2) * 0.42 / 1 * 0.29'
+ as='int((1 + 2)/2) * 0.42 / 1 * 0.29' pd='2*int((1 + 1)/2) * (0.42 / 1 + 0.29)' ps='2*int((1 + 2)/2) * (0.42 / 1 + 0.29)'
+ nrd='0.29 / 0.42 ' nrs='0.29 / 0.42 ' sa=0 sb=0 sd=0 mult=1 m=1
.ends


* expanding   symbol:  LELO_SVOD_SKY130A/XGL6030-822_sat.sym # of pins=2
** sym_path: design/LELO_SVOD_SKY130A/XGL6030-822_sat.sym

.subckt XGL6030-822_sat port1 port2
X1 port1 port2 Model1C R1=5 R2=0.04 C= 15.2p K1=0.000001 K2=2 K3= 8.2u K4=0.000001 K5=0.000001
+ L=8.1093E-06 Is=13.9236 a=0.7109 L_Z0=0 L_EL=0 L_F0=0E6 PkZ=7057.14402
.ends XGL6030-822_sat


* expanding   symbol:  LELO_SVOD_SKY130A/LELO_RING_DEL_VC.sym # of pins=6
** sym_path: design/LELO_SVOD_SKY130A/LELO_RING_DEL_VC.sym
** sch_path: design/LELO_SVOD_SKY130A/LELO_RING_DEL_VC.sch
.subckt LELO_RING_DEL_VC VDD VC2 VIN VOUT VC GND
*.ipin VIN
*.ipin VDD
*.ipin GND
*.opin VOUT
*.ipin VC
*.ipin VC2
XM1 net2 VC2 VDD VDD sky130_fd_pr__pfet_01v8 L=5 W=0.42 nf=1 ad='int((1 + 1)/2) * 0.42 / 1 * 0.29' as='int((1 + 2)/2) * 0.42 / 1 * 0.29'
+ pd='2*int((1 + 1)/2) * (0.42 / 1 + 0.29)' ps='2*int((1 + 2)/2) * (0.42 / 1 + 0.29)' nrd='0.29 / 0.42 '
+ nrs='0.29 / 0.42 ' sa=0 sb=0 sd=0 mult=1 m=1
XM2 VOUT VIN net2 net2 sky130_fd_pr__pfet_01v8 L=5 W=0.42 nf=1 ad='int((1 + 1)/2) * 0.42 / 1 * 0.29'
+ as='int((1 + 2)/2) * 0.42 / 1 * 0.29' pd='2*int((1 + 1)/2) * (0.42 / 1 + 0.29)' ps='2*int((1 + 2)/2) * (0.42 / 1 + 0.29)'
+ nrd='0.29 / 0.42 ' nrs='0.29 / 0.42 ' sa=0 sb=0 sd=0 mult=1 m=1
XM3 VOUT VIN net1 GND sky130_fd_pr__nfet_01v8 L=5 W=0.42 nf=1 ad='int((1 + 1)/2) * 0.42 / 1 * 0.29' as='int((1 + 2)/2) * 0.42 / 1 * 0.29'
+ pd='2*int((1 + 1)/2) * (0.42 / 1 + 0.29)' ps='2*int((1 + 2)/2) * (0.42 / 1 + 0.29)' nrd='0.29 / 0.42 '
+ nrs='0.29 / 0.42 ' sa=0 sb=0 sd=0 mult=1 m=1
XM4 net1 VC GND GND sky130_fd_pr__nfet_01v8 L=5 W=0.42 nf=1 ad='int((1 + 1)/2) * 0.42 / 1 * 0.29' as='int((1 + 2)/2) * 0.42 / 1 * 0.29'
+ pd='2*int((1 + 1)/2) * (0.42 / 1 + 0.29)' ps='2*int((1 + 2)/2) * (0.42 / 1 + 0.29)' nrd='0.29 / 0.42 '
+ nrs='0.29 / 0.42 ' sa=0 sb=0 sd=0 mult=1 m=1
.ends

.end
